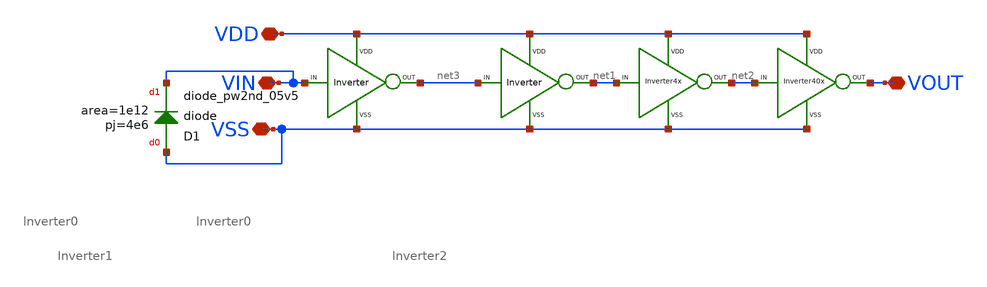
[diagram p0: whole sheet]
** sch_path: xschem/DC_DC_Converter_xschem/DC_DC_Converter/BUFFER/BUFFER_PMOS/BUFFER_P.sch
**.subckt BUFFER_P VDD VIN VSS VOUT
*.iopin VDD
*.iopin VIN
*.iopin VSS
*.iopin VOUT
X7 net3 net1 VDD VSS Inverter0
X8 net1 net2 VDD VSS Inverter1
X1 net2 VOUT VDD VSS Inverter2
X2 VIN net3 VDD VSS Inverter0
XD1 VSS VIN sky130_fd_pr__diode_pw2nd_05v5 area=1e12 pj=4e6
**.ends
.end
